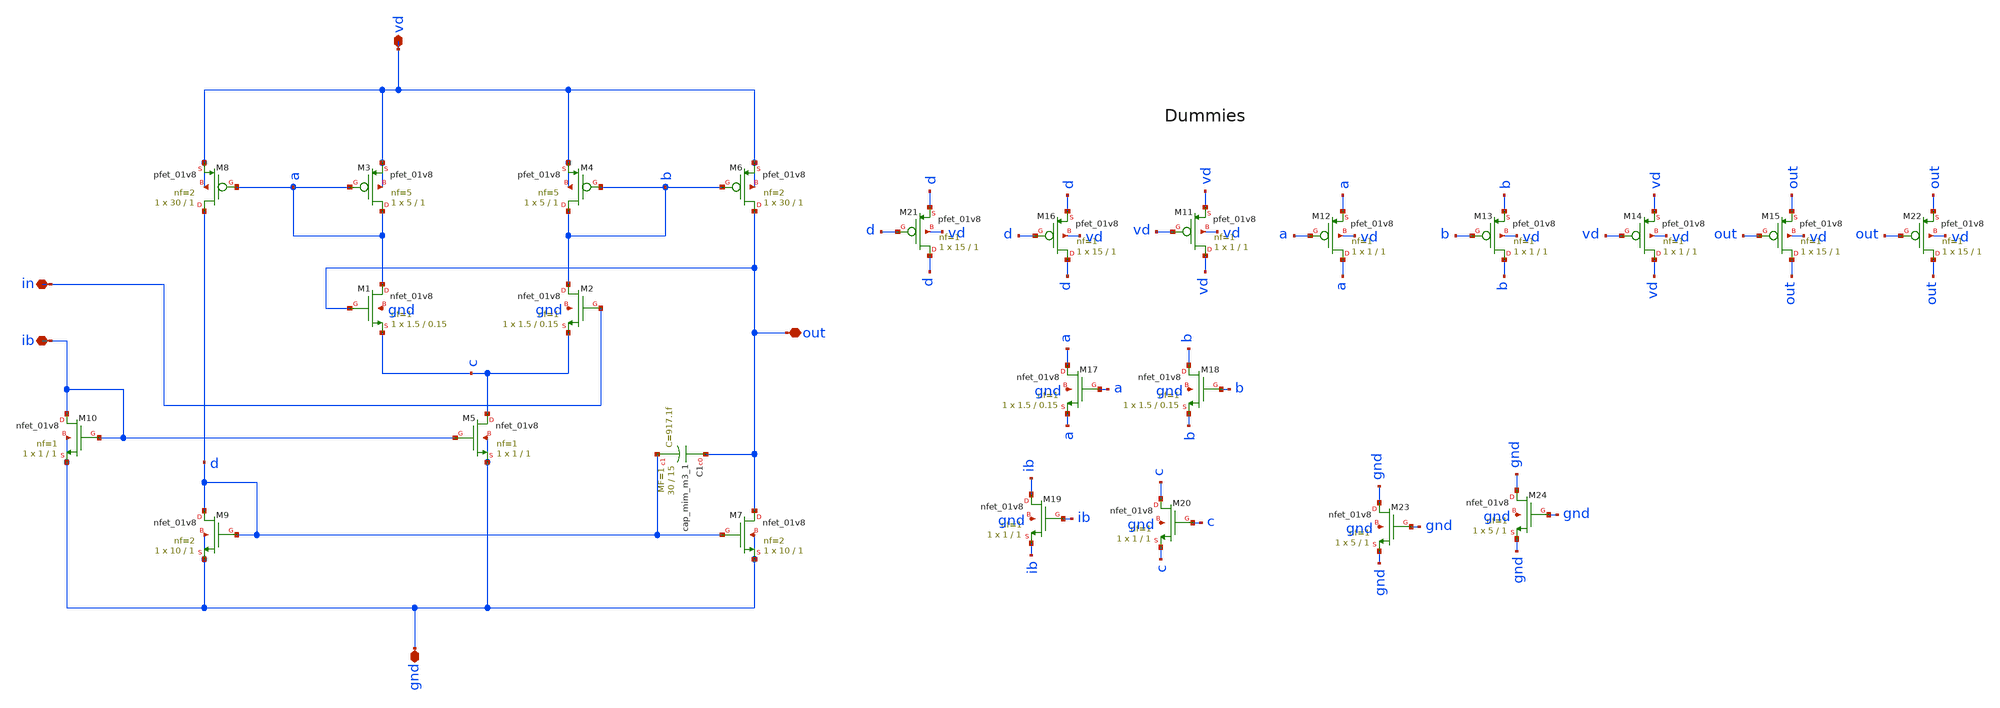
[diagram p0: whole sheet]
** sch_path: buffer/xschem/buffer.sch
* Copyright 2020 Stefan Frederik Schippers
* Licensed under the Apache License, Version 2.0 (the "License");
* you may not use this file except in compliance with the License.
* You may obtain a copy of the License at
* https://www.apache.org/licenses/LICENSE-2.0
* Unless required by applicable law or agreed to in writing, software
* distributed under the License is distributed on an "AS IS" BASIS,
* WITHOUT WARRANTIES OR CONDITIONS OF ANY KIND, either express or implied.
* See the License for the specific language governing permissions and
* limitations under the License.
**.subckt buffer vd ib out in gnd
*.iopin vd
*.iopin ib
*.iopin out
*.iopin in
*.iopin gnd
XM3 a a vd vd sky130_fd_pr__pfet_01v8 L=1 W=5 nf=5 ad='int((nf+1)/2) * W/nf * 0.29' as='int((nf+2)/2) * W/nf * 0.29'
+ pd='2*int((nf+1)/2) * (W/nf + 0.29)' ps='2*int((nf+2)/2) * (W/nf + 0.29)' nrd='0.29 / W' nrs='0.29 / W'
+ sa=0 sb=0 sd=0 mult=1 m=1
XM1 a out c gnd sky130_fd_pr__nfet_01v8 L=0.15 W=1.5 nf=1 ad='int((nf+1)/2) * W/nf * 0.29' as='int((nf+2)/2) * W/nf * 0.29'
+ pd='2*int((nf+1)/2) * (W/nf + 0.29)' ps='2*int((nf+2)/2) * (W/nf + 0.29)' nrd='0.29 / W' nrs='0.29 / W'
+ sa=0 sb=0 sd=0 mult=1 m=1
XM2 b in c gnd sky130_fd_pr__nfet_01v8 L=0.15 W=1.5 nf=1 ad='int((nf+1)/2) * W/nf * 0.29' as='int((nf+2)/2) * W/nf * 0.29'
+ pd='2*int((nf+1)/2) * (W/nf + 0.29)' ps='2*int((nf+2)/2) * (W/nf + 0.29)' nrd='0.29 / W' nrs='0.29 / W'
+ sa=0 sb=0 sd=0 mult=1 m=1
XM4 b b vd vd sky130_fd_pr__pfet_01v8 L=1 W=5 nf=5 ad='int((nf+1)/2) * W/nf * 0.29' as='int((nf+2)/2) * W/nf * 0.29'
+ pd='2*int((nf+1)/2) * (W/nf + 0.29)' ps='2*int((nf+2)/2) * (W/nf + 0.29)' nrd='0.29 / W' nrs='0.29 / W'
+ sa=0 sb=0 sd=0 mult=1 m=1
XM5 c ib gnd gnd sky130_fd_pr__nfet_01v8 L=1 W=1 nf=1 ad='int((nf+1)/2) * W/nf * 0.29' as='int((nf+2)/2) * W/nf * 0.29'
+ pd='2*int((nf+1)/2) * (W/nf + 0.29)' ps='2*int((nf+2)/2) * (W/nf + 0.29)' nrd='0.29 / W' nrs='0.29 / W'
+ sa=0 sb=0 sd=0 mult=1 m=1
XM6 out b vd vd sky130_fd_pr__pfet_01v8 L=1 W=30 nf=2 ad='int((nf+1)/2) * W/nf * 0.29' as='int((nf+2)/2) * W/nf * 0.29'
+ pd='2*int((nf+1)/2) * (W/nf + 0.29)' ps='2*int((nf+2)/2) * (W/nf + 0.29)' nrd='0.29 / W' nrs='0.29 / W'
+ sa=0 sb=0 sd=0 mult=1 m=1
XM7 out d gnd gnd sky130_fd_pr__nfet_01v8 L=1 W=10 nf=2 ad='int((nf+1)/2) * W/nf * 0.29' as='int((nf+2)/2) * W/nf * 0.29'
+ pd='2*int((nf+1)/2) * (W/nf + 0.29)' ps='2*int((nf+2)/2) * (W/nf + 0.29)' nrd='0.29 / W' nrs='0.29 / W'
+ sa=0 sb=0 sd=0 mult=1 m=1
XM8 d a vd vd sky130_fd_pr__pfet_01v8 L=1 W=30 nf=2 ad='int((nf+1)/2) * W/nf * 0.29' as='int((nf+2)/2) * W/nf * 0.29'
+ pd='2*int((nf+1)/2) * (W/nf + 0.29)' ps='2*int((nf+2)/2) * (W/nf + 0.29)' nrd='0.29 / W' nrs='0.29 / W'
+ sa=0 sb=0 sd=0 mult=1 m=1
XM9 d d gnd gnd sky130_fd_pr__nfet_01v8 L=1 W=10 nf=2 ad='int((nf+1)/2) * W/nf * 0.29' as='int((nf+2)/2) * W/nf * 0.29'
+ pd='2*int((nf+1)/2) * (W/nf + 0.29)' ps='2*int((nf+2)/2) * (W/nf + 0.29)' nrd='0.29 / W' nrs='0.29 / W'
+ sa=0 sb=0 sd=0 mult=1 m=1
XM10 ib ib gnd gnd sky130_fd_pr__nfet_01v8 L=1 W=1 nf=1 ad='int((nf+1)/2) * W/nf * 0.29' as='int((nf+2)/2) * W/nf * 0.29'
+ pd='2*int((nf+1)/2) * (W/nf + 0.29)' ps='2*int((nf+2)/2) * (W/nf + 0.29)' nrd='0.29 / W' nrs='0.29 / W'
+ sa=0 sb=0 sd=0 mult=1 m=1
XM11 vd vd vd vd sky130_fd_pr__pfet_01v8 L=1 W=1 nf=1 ad='int((nf+1)/2) * W/nf * 0.29' as='int((nf+2)/2) * W/nf * 0.29'
+ pd='2*int((nf+1)/2) * (W/nf + 0.29)' ps='2*int((nf+2)/2) * (W/nf + 0.29)' nrd='0.29 / W' nrs='0.29 / W'
+ sa=0 sb=0 sd=0 mult=1 m=1
XM12 a a a vd sky130_fd_pr__pfet_01v8 L=1 W=1 nf=1 ad='int((nf+1)/2) * W/nf * 0.29' as='int((nf+2)/2) * W/nf * 0.29'
+ pd='2*int((nf+1)/2) * (W/nf + 0.29)' ps='2*int((nf+2)/2) * (W/nf + 0.29)' nrd='0.29 / W' nrs='0.29 / W'
+ sa=0 sb=0 sd=0 mult=1 m=1
XM13 b b b vd sky130_fd_pr__pfet_01v8 L=1 W=1 nf=1 ad='int((nf+1)/2) * W/nf * 0.29' as='int((nf+2)/2) * W/nf * 0.29'
+ pd='2*int((nf+1)/2) * (W/nf + 0.29)' ps='2*int((nf+2)/2) * (W/nf + 0.29)' nrd='0.29 / W' nrs='0.29 / W'
+ sa=0 sb=0 sd=0 mult=1 m=1
XM14 vd vd vd vd sky130_fd_pr__pfet_01v8 L=1 W=1 nf=1 ad='int((nf+1)/2) * W/nf * 0.29' as='int((nf+2)/2) * W/nf * 0.29'
+ pd='2*int((nf+1)/2) * (W/nf + 0.29)' ps='2*int((nf+2)/2) * (W/nf + 0.29)' nrd='0.29 / W' nrs='0.29 / W'
+ sa=0 sb=0 sd=0 mult=1 m=1
XM15 out out out vd sky130_fd_pr__pfet_01v8 L=1 W=15 nf=1 ad='int((nf+1)/2) * W/nf * 0.29' as='int((nf+2)/2) * W/nf * 0.29'
+ pd='2*int((nf+1)/2) * (W/nf + 0.29)' ps='2*int((nf+2)/2) * (W/nf + 0.29)' nrd='0.29 / W' nrs='0.29 / W'
+ sa=0 sb=0 sd=0 mult=1 m=1
XM16 d d d vd sky130_fd_pr__pfet_01v8 L=1 W=15 nf=1 ad='int((nf+1)/2) * W/nf * 0.29' as='int((nf+2)/2) * W/nf * 0.29'
+ pd='2*int((nf+1)/2) * (W/nf + 0.29)' ps='2*int((nf+2)/2) * (W/nf + 0.29)' nrd='0.29 / W' nrs='0.29 / W'
+ sa=0 sb=0 sd=0 mult=1 m=1
XM17 a a a gnd sky130_fd_pr__nfet_01v8 L=0.15 W=1.5 nf=1 ad='int((nf+1)/2) * W/nf * 0.29' as='int((nf+2)/2) * W/nf * 0.29'
+ pd='2*int((nf+1)/2) * (W/nf + 0.29)' ps='2*int((nf+2)/2) * (W/nf + 0.29)' nrd='0.29 / W' nrs='0.29 / W'
+ sa=0 sb=0 sd=0 mult=1 m=1
XM18 b b b gnd sky130_fd_pr__nfet_01v8 L=0.15 W=1.5 nf=1 ad='int((nf+1)/2) * W/nf * 0.29' as='int((nf+2)/2) * W/nf * 0.29'
+ pd='2*int((nf+1)/2) * (W/nf + 0.29)' ps='2*int((nf+2)/2) * (W/nf + 0.29)' nrd='0.29 / W' nrs='0.29 / W'
+ sa=0 sb=0 sd=0 mult=1 m=1
XM19 ib ib ib gnd sky130_fd_pr__nfet_01v8 L=1 W=1 nf=1 ad='int((nf+1)/2) * W/nf * 0.29' as='int((nf+2)/2) * W/nf * 0.29'
+ pd='2*int((nf+1)/2) * (W/nf + 0.29)' ps='2*int((nf+2)/2) * (W/nf + 0.29)' nrd='0.29 / W' nrs='0.29 / W'
+ sa=0 sb=0 sd=0 mult=1 m=1
XM20 c c c gnd sky130_fd_pr__nfet_01v8 L=1 W=1 nf=1 ad='int((nf+1)/2) * W/nf * 0.29' as='int((nf+2)/2) * W/nf * 0.29'
+ pd='2*int((nf+1)/2) * (W/nf + 0.29)' ps='2*int((nf+2)/2) * (W/nf + 0.29)' nrd='0.29 / W' nrs='0.29 / W'
+ sa=0 sb=0 sd=0 mult=1 m=1
XM21 d d d vd sky130_fd_pr__pfet_01v8 L=1 W=15 nf=1 ad='int((nf+1)/2) * W/nf * 0.29' as='int((nf+2)/2) * W/nf * 0.29'
+ pd='2*int((nf+1)/2) * (W/nf + 0.29)' ps='2*int((nf+2)/2) * (W/nf + 0.29)' nrd='0.29 / W' nrs='0.29 / W'
+ sa=0 sb=0 sd=0 mult=1 m=1
XM22 out out out vd sky130_fd_pr__pfet_01v8 L=1 W=15 nf=1 ad='int((nf+1)/2) * W/nf * 0.29' as='int((nf+2)/2) * W/nf * 0.29'
+ pd='2*int((nf+1)/2) * (W/nf + 0.29)' ps='2*int((nf+2)/2) * (W/nf + 0.29)' nrd='0.29 / W' nrs='0.29 / W'
+ sa=0 sb=0 sd=0 mult=1 m=1
XM23 gnd gnd gnd gnd sky130_fd_pr__nfet_01v8 L=1 W=5 nf=1 ad='int((nf+1)/2) * W/nf * 0.29' as='int((nf+2)/2) * W/nf * 0.29'
+ pd='2*int((nf+1)/2) * (W/nf + 0.29)' ps='2*int((nf+2)/2) * (W/nf + 0.29)' nrd='0.29 / W' nrs='0.29 / W'
+ sa=0 sb=0 sd=0 mult=1 m=1
XM24 gnd gnd gnd gnd sky130_fd_pr__nfet_01v8 L=1 W=5 nf=1 ad='int((nf+1)/2) * W/nf * 0.29' as='int((nf+2)/2) * W/nf * 0.29'
+ pd='2*int((nf+1)/2) * (W/nf + 0.29)' ps='2*int((nf+2)/2) * (W/nf + 0.29)' nrd='0.29 / W' nrs='0.29 / W'
+ sa=0 sb=0 sd=0 mult=1 m=1
XC1 out d sky130_fd_pr__cap_mim_m3_1 W=30 L=15 MF=1 m=1
**.ends
.end
